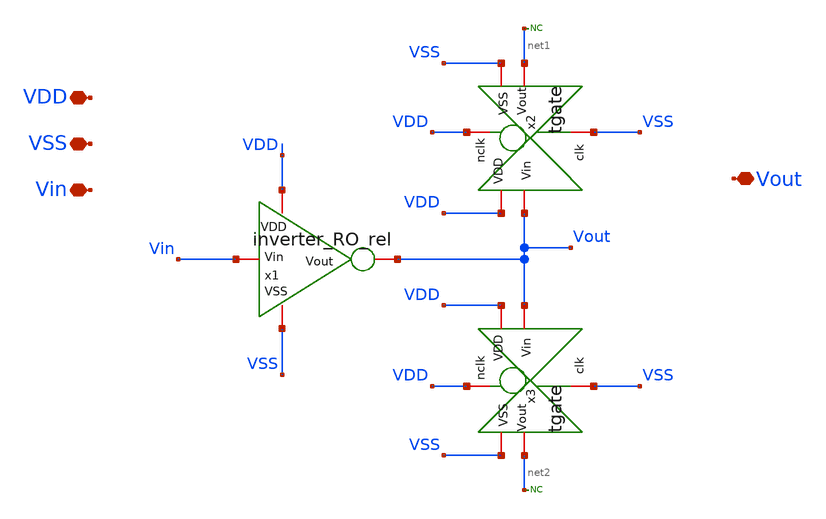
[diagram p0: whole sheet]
** sch_path: TT/rovcel2.sch
**.subckt rovcel2 VDD VSS Vin Vout
*.iopin VDD
*.iopin VSS
*.iopin Vin
*.iopin Vout
x1 VDD Vin Vout VSS inverter_RO_rel
x2 VDD VDD Vout net1 VSS VSS tgate
x3 VDD VDD Vout net2 VSS VSS tgate
* noconn #net1
* noconn #net2
**.ends

* expanding   symbol:  /foss/designs/Projects/RO_reliability/xschem/inverter_RO_rel.sym # of pins=4
** sym_path: TT/inverter_RO_rel.sym
** sch_path: TT/inverter_RO_rel.sch
.subckt inverter_RO_rel VDD Vin Vout VSS
*.iopin VDD
*.iopin VSS
*.iopin Vin
*.iopin Vout
XM2 Vout Vin VDD VDD sky130_fd_pr__pfet_01v8 L=0.15 W=4.75 nf=1 ad='int((nf+1)/2) * W/nf * 0.29' as='int((nf+2)/2) * W/nf * 0.29'
+ pd='2*int((nf+1)/2) * (W/nf + 0.29)' ps='2*int((nf+2)/2) * (W/nf + 0.29)' nrd='0.29 / W' nrs='0.29 / W'
+ sa=0 sb=0 sd=0 mult=4 m=4
XM1 Vout Vin VSS VSS sky130_fd_pr__nfet_01v8 L=0.15 W=2.1 nf=1 ad='int((nf+1)/2) * W/nf * 0.29' as='int((nf+2)/2) * W/nf * 0.29'
+ pd='2*int((nf+1)/2) * (W/nf + 0.29)' ps='2*int((nf+2)/2) * (W/nf + 0.29)' nrd='0.29 / W' nrs='0.29 / W'
+ sa=0 sb=0 sd=0 mult=2 m=2
.ends


* expanding   symbol:  /foss/designs/Projects/RO_reliability/xschem/tgate.sym # of pins=6
** sym_path: TT/tgate.sym
** sch_path: TT/tgate.sch
.subckt tgate nclk VDD Vin Vout VSS clk
*.iopin nclk
*.iopin clk
*.iopin VDD
*.iopin VSS
*.iopin Vout
*.iopin Vin
XM1 Vin nclk Vout VDD sky130_fd_pr__pfet_01v8 L=0.15 W=0.45 nf=1 ad='int((nf+1)/2) * W/nf * 0.29' as='int((nf+2)/2) * W/nf * 0.29'
+ pd='2*int((nf+1)/2) * (W/nf + 0.29)' ps='2*int((nf+2)/2) * (W/nf + 0.29)' nrd='0.29 / W' nrs='0.29 / W'
+ sa=0 sb=0 sd=0 mult=1 m=1
XM2 Vin clk Vout VSS sky130_fd_pr__nfet_01v8 L=0.15 W=0.45 nf=1 ad='int((nf+1)/2) * W/nf * 0.29' as='int((nf+2)/2) * W/nf * 0.29'
+ pd='2*int((nf+1)/2) * (W/nf + 0.29)' ps='2*int((nf+2)/2) * (W/nf + 0.29)' nrd='0.29 / W' nrs='0.29 / W'
+ sa=0 sb=0 sd=0 mult=1 m=1
.ends

.end
